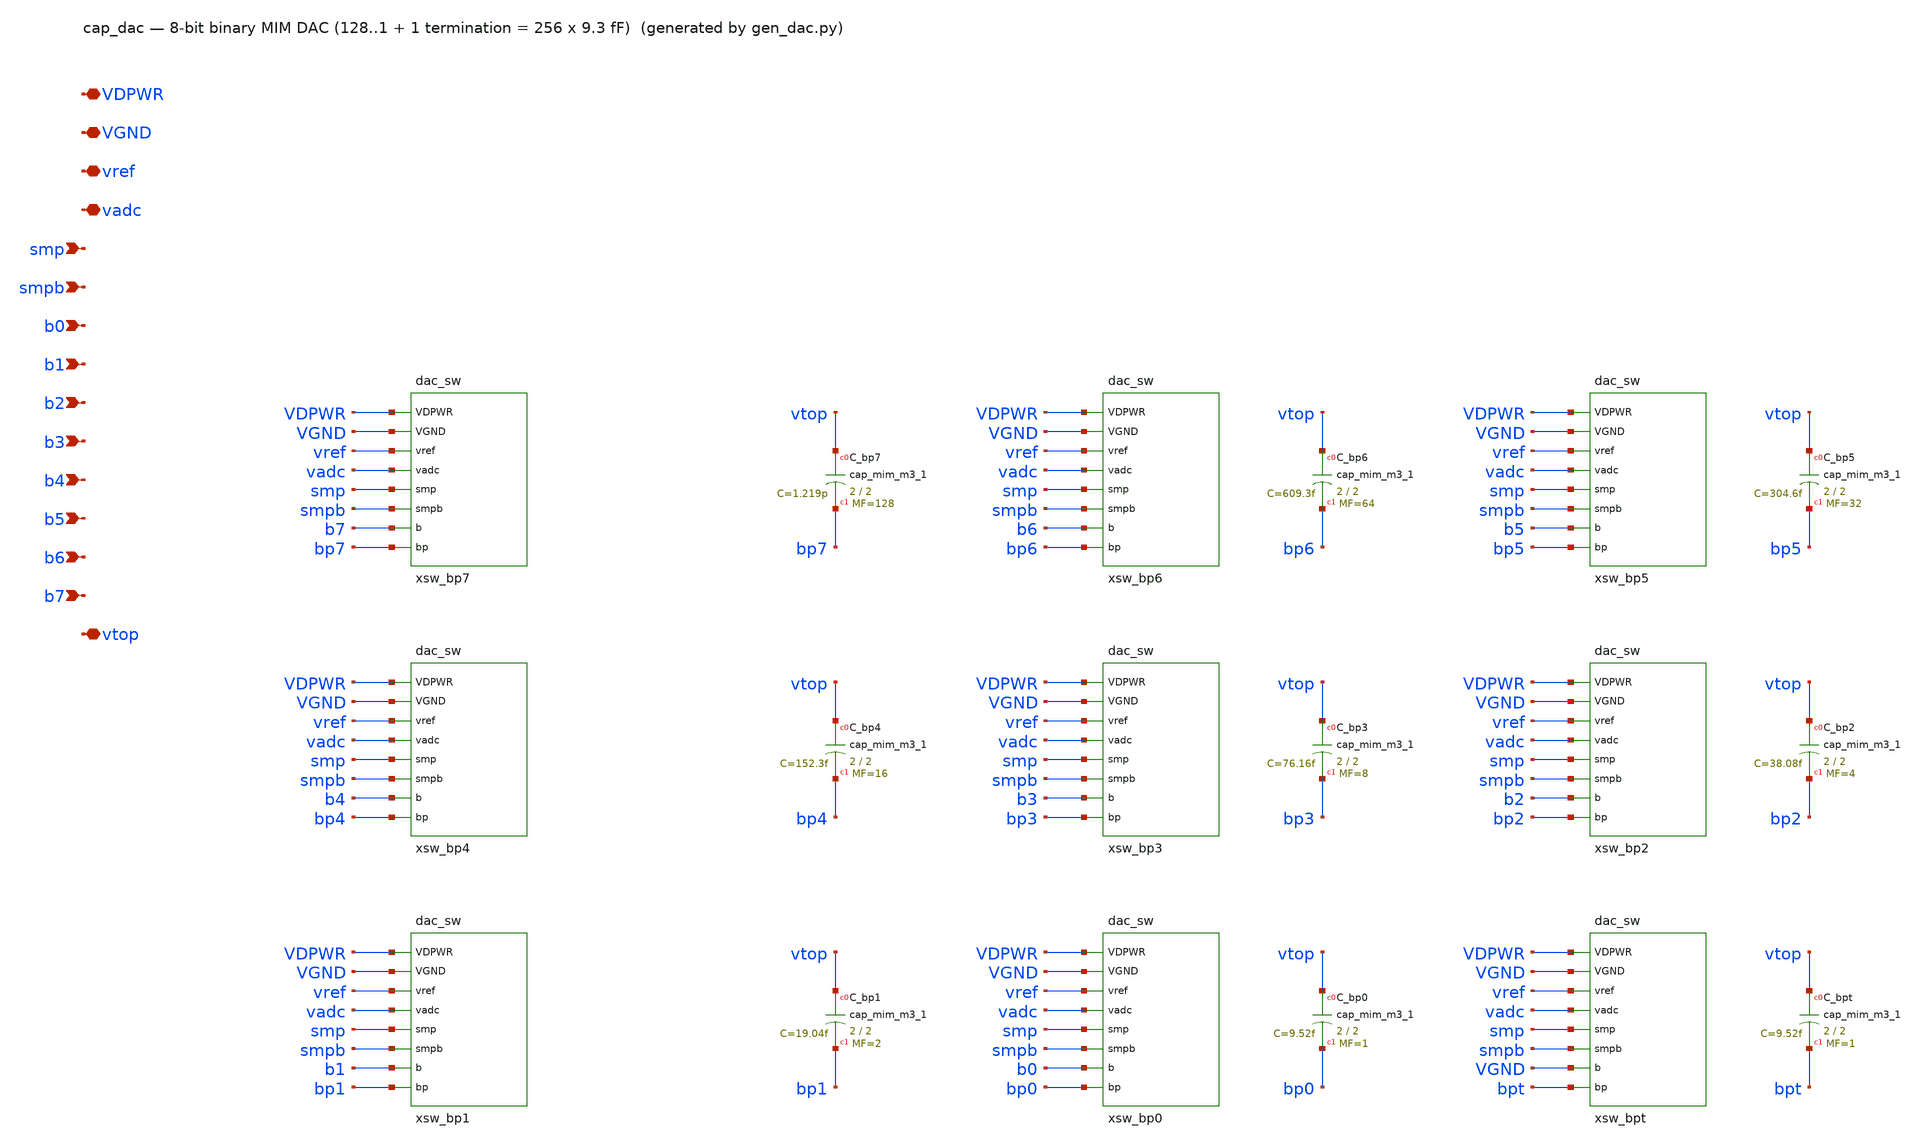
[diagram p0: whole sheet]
** sch_path: xschem/cap_dac.sch
**.subckt cap_dac VDPWR VGND vref vadc smp smpb b0 b1 b2 b3 b4 b5 b6 b7 vtop
*.iopin VDPWR
*.iopin VGND
*.iopin vref
*.iopin vadc
*.ipin smp
*.ipin smpb
*.ipin b0
*.ipin b1
*.ipin b2
*.ipin b3
*.ipin b4
*.ipin b5
*.ipin b6
*.ipin b7
*.iopin vtop
xsw_bp7 VDPWR VGND vref vadc smp smpb b7 bp7 dac_sw
XC_bp7 vtop bp7 sky130_fd_pr__cap_mim_m3_1 W=2 L=2 MF=128 m=128
xsw_bp6 VDPWR VGND vref vadc smp smpb b6 bp6 dac_sw
XC_bp6 vtop bp6 sky130_fd_pr__cap_mim_m3_1 W=2 L=2 MF=64 m=64
xsw_bp5 VDPWR VGND vref vadc smp smpb b5 bp5 dac_sw
XC_bp5 vtop bp5 sky130_fd_pr__cap_mim_m3_1 W=2 L=2 MF=32 m=32
xsw_bp4 VDPWR VGND vref vadc smp smpb b4 bp4 dac_sw
XC_bp4 vtop bp4 sky130_fd_pr__cap_mim_m3_1 W=2 L=2 MF=16 m=16
xsw_bp3 VDPWR VGND vref vadc smp smpb b3 bp3 dac_sw
XC_bp3 vtop bp3 sky130_fd_pr__cap_mim_m3_1 W=2 L=2 MF=8 m=8
xsw_bp2 VDPWR VGND vref vadc smp smpb b2 bp2 dac_sw
XC_bp2 vtop bp2 sky130_fd_pr__cap_mim_m3_1 W=2 L=2 MF=4 m=4
xsw_bp1 VDPWR VGND vref vadc smp smpb b1 bp1 dac_sw
XC_bp1 vtop bp1 sky130_fd_pr__cap_mim_m3_1 W=2 L=2 MF=2 m=2
xsw_bp0 VDPWR VGND vref vadc smp smpb b0 bp0 dac_sw
XC_bp0 vtop bp0 sky130_fd_pr__cap_mim_m3_1 W=2 L=2 MF=1 m=1
xsw_bpt VDPWR VGND vref vadc smp smpb VGND bpt dac_sw
XC_bpt vtop bpt sky130_fd_pr__cap_mim_m3_1 W=2 L=2 MF=1 m=1
**.ends

* expanding   symbol:  dac_sw.sym # of pins=8
** sym_path: xschem/dac_sw.sym
** sch_path: xschem/dac_sw.sch
.subckt dac_sw VDPWR VGND vref vadc smp smpb b bp
*.iopin VDPWR
*.iopin VGND
*.iopin vref
*.iopin vadc
*.ipin smp
*.ipin smpb
*.ipin b
*.iopin bp
XMNRA mnr smp VDPWR VDPWR sky130_fd_pr__pfet_01v8 L=0.15 W=1.68 nf=1 ad='int((nf+1)/2) * W/nf * 0.29'
+ as='int((nf+2)/2) * W/nf * 0.29' pd='2*int((nf+1)/2) * (W/nf + 0.29)' ps='2*int((nf+2)/2) * (W/nf + 0.29)'
+ nrd='0.29 / W' nrs='0.29 / W' sa=0 sb=0 sd=0 mult=1 m=1
XMNRB gn b mnr VDPWR sky130_fd_pr__pfet_01v8 L=0.15 W=1.68 nf=1 ad='int((nf+1)/2) * W/nf * 0.29' as='int((nf+2)/2) * W/nf * 0.29'
+ pd='2*int((nf+1)/2) * (W/nf + 0.29)' ps='2*int((nf+2)/2) * (W/nf + 0.29)' nrd='0.29 / W' nrs='0.29 / W'
+ sa=0 sb=0 sd=0 mult=1 m=1
XMNRC gn smp VGND VGND sky130_fd_pr__nfet_01v8 L=0.15 W=0.42 nf=1 ad='int((1 + 1)/2) * 0.42 / 1 * 0.29'
+ as='int((1 + 2)/2) * 0.42 / 1 * 0.29' pd='2*int((1 + 1)/2) * (0.42 / 1 + 0.29)' ps='2*int((1 + 2)/2) * (0.42 / 1 + 0.29)'
+ nrd='0.29 / 0.42 ' nrs='0.29 / 0.42 ' sa=0 sb=0 sd=0 mult=1 m=1
XMNRD gn b VGND VGND sky130_fd_pr__nfet_01v8 L=0.15 W=0.42 nf=1 ad='int((1 + 1)/2) * 0.42 / 1 * 0.29'
+ as='int((1 + 2)/2) * 0.42 / 1 * 0.29' pd='2*int((1 + 1)/2) * (0.42 / 1 + 0.29)' ps='2*int((1 + 2)/2) * (0.42 / 1 + 0.29)'
+ nrd='0.29 / 0.42 ' nrs='0.29 / 0.42 ' sa=0 sb=0 sd=0 mult=1 m=1
XMNDA gpb smpb VDPWR VDPWR sky130_fd_pr__pfet_01v8 L=0.15 W=0.84 nf=1 ad='int((nf+1)/2) * W/nf * 0.29'
+ as='int((nf+2)/2) * W/nf * 0.29' pd='2*int((nf+1)/2) * (W/nf + 0.29)' ps='2*int((nf+2)/2) * (W/nf + 0.29)'
+ nrd='0.29 / W' nrs='0.29 / W' sa=0 sb=0 sd=0 mult=1 m=1
XMNDB gpb b VDPWR VDPWR sky130_fd_pr__pfet_01v8 L=0.15 W=0.84 nf=1 ad='int((nf+1)/2) * W/nf * 0.29' as='int((nf+2)/2) * W/nf * 0.29'
+ pd='2*int((nf+1)/2) * (W/nf + 0.29)' ps='2*int((nf+2)/2) * (W/nf + 0.29)' nrd='0.29 / W' nrs='0.29 / W'
+ sa=0 sb=0 sd=0 mult=1 m=1
XMNDC gpb smpb mnd VGND sky130_fd_pr__nfet_01v8 L=0.15 W=0.84 nf=1 ad='int((1 + 1)/2) * 0.84 / 1 * 0.29'
+ as='int((1 + 2)/2) * 0.84 / 1 * 0.29' pd='2*int((1 + 1)/2) * (0.84 / 1 + 0.29)' ps='2*int((1 + 2)/2) * (0.84 / 1 + 0.29)'
+ nrd='0.29 / 0.84 ' nrs='0.29 / 0.84 ' sa=0 sb=0 sd=0 mult=1 m=1
XMNDD mnd b VGND VGND sky130_fd_pr__nfet_01v8 L=0.15 W=0.84 nf=1 ad='int((1 + 1)/2) * 0.84 / 1 * 0.29'
+ as='int((1 + 2)/2) * 0.84 / 1 * 0.29' pd='2*int((1 + 1)/2) * (0.84 / 1 + 0.29)' ps='2*int((1 + 2)/2) * (0.84 / 1 + 0.29)'
+ nrd='0.29 / 0.84 ' nrs='0.29 / 0.84 ' sa=0 sb=0 sd=0 mult=1 m=1
XMSG bp gn VGND VGND sky130_fd_pr__nfet_01v8 L=0.15 W=1 nf=1 ad='int((1 + 1)/2) * 1 / 1 * 0.29' as='int((1 + 2)/2) * 1 / 1 * 0.29'
+ pd='2*int((1 + 1)/2) * (1 / 1 + 0.29)' ps='2*int((1 + 2)/2) * (1 / 1 + 0.29)' nrd='0.29 / 1 ' nrs='0.29 / 1 '
+ sa=0 sb=0 sd=0 mult=1 m=1
XMSR bp gpb vref VDPWR sky130_fd_pr__pfet_01v8_lvt L=0.35 W=4 nf=1 ad='int((1 + 1)/2) * 4 / 1 * 0.29'
+ as='int((1 + 2)/2) * 4 / 1 * 0.29' pd='2*int((1 + 1)/2) * (4 / 1 + 0.29)' ps='2*int((1 + 2)/2) * (4 / 1 + 0.29)'
+ nrd='0.29 / 4 ' nrs='0.29 / 4 ' sa=0 sb=0 sd=0 mult=1 m=1
XMSN bp smp vadc VGND sky130_fd_pr__nfet_01v8 L=0.15 W=1 nf=1 ad='int((1 + 1)/2) * 1 / 1 * 0.29' as='int((1 + 2)/2) * 1 / 1 * 0.29'
+ pd='2*int((1 + 1)/2) * (1 / 1 + 0.29)' ps='2*int((1 + 2)/2) * (1 / 1 + 0.29)' nrd='0.29 / 1 ' nrs='0.29 / 1 '
+ sa=0 sb=0 sd=0 mult=1 m=1
XMSP bp smpb vadc VDPWR sky130_fd_pr__pfet_01v8_lvt L=0.35 W=2 nf=1 ad='int((1 + 1)/2) * 2 / 1 * 0.29'
+ as='int((1 + 2)/2) * 2 / 1 * 0.29' pd='2*int((1 + 1)/2) * (2 / 1 + 0.29)' ps='2*int((1 + 2)/2) * (2 / 1 + 0.29)'
+ nrd='0.29 / 2 ' nrs='0.29 / 2 ' sa=0 sb=0 sd=0 mult=1 m=1
.ends

.end
